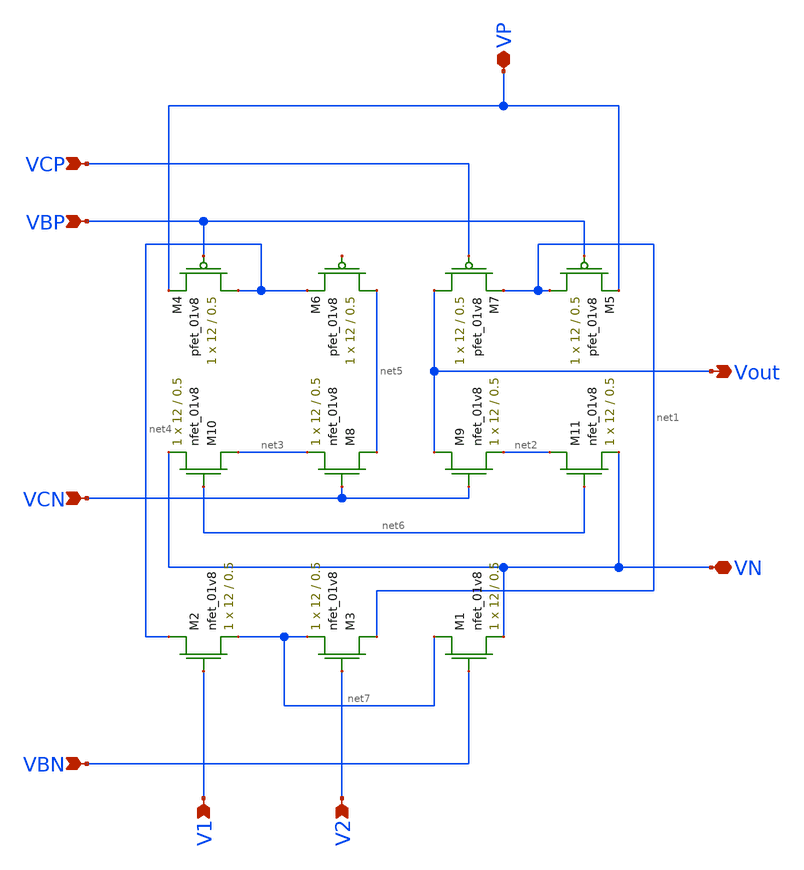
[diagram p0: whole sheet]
** sch_path: mp3/diff_amp/diff_amp_LDS_v1.sch
**.subckt diff_amp_LDS_v1 V1 V2 VN VBN VBP VP VCP VCN Vout
*.ipin V1
*.ipin V2
*.iopin VN
*.ipin VBN
*.ipin VBP
*.iopin VP
*.ipin VCP
*.ipin VCN
*.opin Vout
XM1 net7 VBN VN VN sky130_fd_pr__nfet_01v8 L=0.5 W=12 nf=1 ad='int((nf+1)/2) * W/nf * 0.29' as='int((nf+2)/2) * W/nf * 0.29'
+ pd='2*int((nf+1)/2) * (W/nf + 0.29)' ps='2*int((nf+2)/2) * (W/nf + 0.29)' nrd='0.29 / W' nrs='0.29 / W'
+ sa=0 sb=0 sd=0 mult=1 m=1
XM2 net4 V1 net7 VN sky130_fd_pr__nfet_01v8 L=0.5 W=12 nf=1 ad='int((nf+1)/2) * W/nf * 0.29' as='int((nf+2)/2) * W/nf * 0.29'
+ pd='2*int((nf+1)/2) * (W/nf + 0.29)' ps='2*int((nf+2)/2) * (W/nf + 0.29)' nrd='0.29 / W' nrs='0.29 / W'
+ sa=0 sb=0 sd=0 mult=1 m=1
XM3 net1 V2 net7 VN sky130_fd_pr__nfet_01v8 L=0.5 W=12 nf=1 ad='int((nf+1)/2) * W/nf * 0.29' as='int((nf+2)/2) * W/nf * 0.29'
+ pd='2*int((nf+1)/2) * (W/nf + 0.29)' ps='2*int((nf+2)/2) * (W/nf + 0.29)' nrd='0.29 / W' nrs='0.29 / W'
+ sa=0 sb=0 sd=0 mult=1 m=1
XM4 net4 VBP VP VP sky130_fd_pr__pfet_01v8 L=0.5 W=12 nf=1 ad='int((nf+1)/2) * W/nf * 0.29' as='int((nf+2)/2) * W/nf * 0.29'
+ pd='2*int((nf+1)/2) * (W/nf + 0.29)' ps='2*int((nf+2)/2) * (W/nf + 0.29)' nrd='0.29 / W' nrs='0.29 / W'
+ sa=0 sb=0 sd=0 mult=1 m=1
XM5 net1 VBP VP VP sky130_fd_pr__pfet_01v8 L=0.5 W=12 nf=1 ad='int((nf+1)/2) * W/nf * 0.29' as='int((nf+2)/2) * W/nf * 0.29'
+ pd='2*int((nf+1)/2) * (W/nf + 0.29)' ps='2*int((nf+2)/2) * (W/nf + 0.29)' nrd='0.29 / W' nrs='0.29 / W'
+ sa=0 sb=0 sd=0 mult=1 m=1
XM6 net5 net8 net4 VP sky130_fd_pr__pfet_01v8 L=0.5 W=12 nf=1 ad='int((nf+1)/2) * W/nf * 0.29' as='int((nf+2)/2) * W/nf * 0.29'
+ pd='2*int((nf+1)/2) * (W/nf + 0.29)' ps='2*int((nf+2)/2) * (W/nf + 0.29)' nrd='0.29 / W' nrs='0.29 / W'
+ sa=0 sb=0 sd=0 mult=1 m=1
XM7 Vout VCP net1 VP sky130_fd_pr__pfet_01v8 L=0.5 W=12 nf=1 ad='int((nf+1)/2) * W/nf * 0.29' as='int((nf+2)/2) * W/nf * 0.29'
+ pd='2*int((nf+1)/2) * (W/nf + 0.29)' ps='2*int((nf+2)/2) * (W/nf + 0.29)' nrd='0.29 / W' nrs='0.29 / W'
+ sa=0 sb=0 sd=0 mult=1 m=1
XM8 net5 VCN net3 VN sky130_fd_pr__nfet_01v8 L=0.5 W=12 nf=1 ad='int((nf+1)/2) * W/nf * 0.29' as='int((nf+2)/2) * W/nf * 0.29'
+ pd='2*int((nf+1)/2) * (W/nf + 0.29)' ps='2*int((nf+2)/2) * (W/nf + 0.29)' nrd='0.29 / W' nrs='0.29 / W'
+ sa=0 sb=0 sd=0 mult=1 m=1
XM9 Vout VCN net2 VN sky130_fd_pr__nfet_01v8 L=0.5 W=12 nf=1 ad='int((nf+1)/2) * W/nf * 0.29' as='int((nf+2)/2) * W/nf * 0.29'
+ pd='2*int((nf+1)/2) * (W/nf + 0.29)' ps='2*int((nf+2)/2) * (W/nf + 0.29)' nrd='0.29 / W' nrs='0.29 / W'
+ sa=0 sb=0 sd=0 mult=1 m=1
XM10 net3 net6 VN VN sky130_fd_pr__nfet_01v8 L=0.5 W=12 nf=1 ad='int((nf+1)/2) * W/nf * 0.29' as='int((nf+2)/2) * W/nf * 0.29'
+ pd='2*int((nf+1)/2) * (W/nf + 0.29)' ps='2*int((nf+2)/2) * (W/nf + 0.29)' nrd='0.29 / W' nrs='0.29 / W'
+ sa=0 sb=0 sd=0 mult=1 m=1
XM11 net2 net6 VN VN sky130_fd_pr__nfet_01v8 L=0.5 W=12 nf=1 ad='int((nf+1)/2) * W/nf * 0.29' as='int((nf+2)/2) * W/nf * 0.29'
+ pd='2*int((nf+1)/2) * (W/nf + 0.29)' ps='2*int((nf+2)/2) * (W/nf + 0.29)' nrd='0.29 / W' nrs='0.29 / W'
+ sa=0 sb=0 sd=0 mult=1 m=1
**.ends
.end
